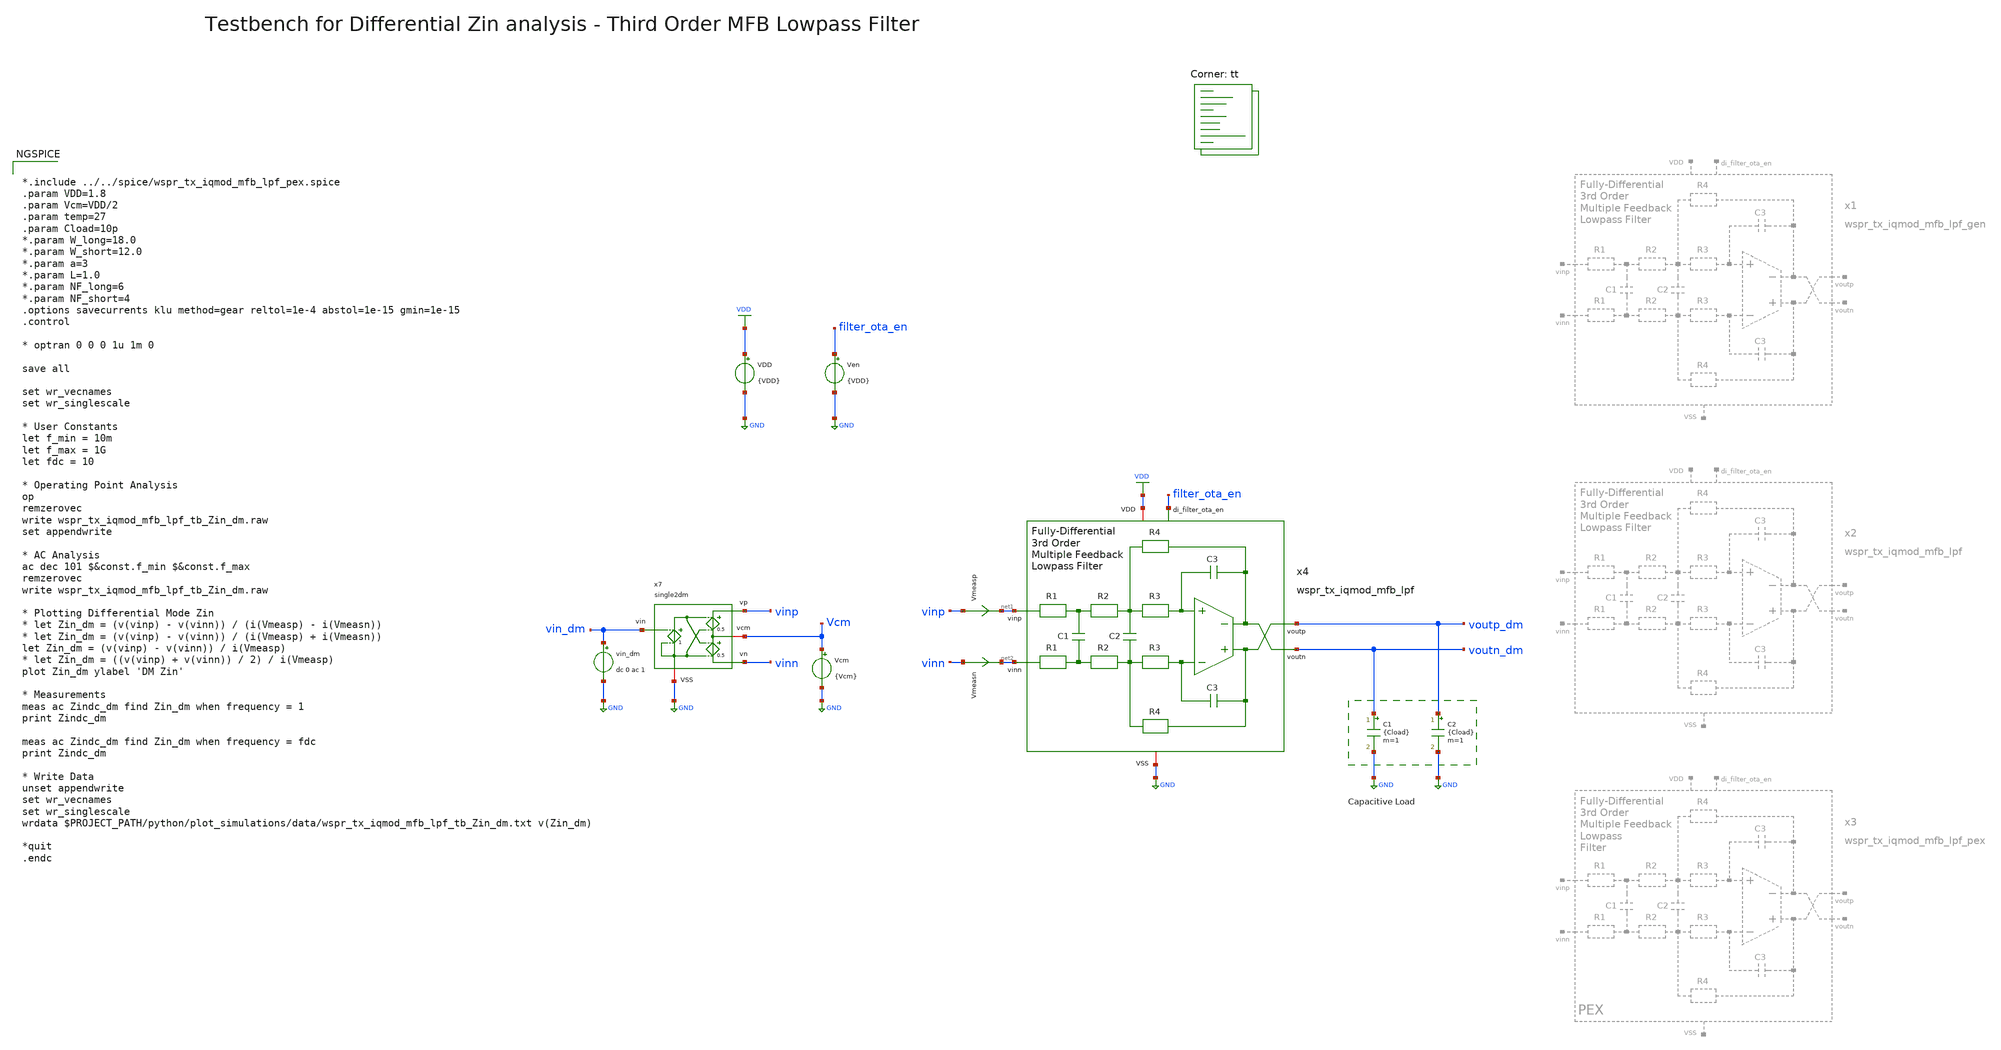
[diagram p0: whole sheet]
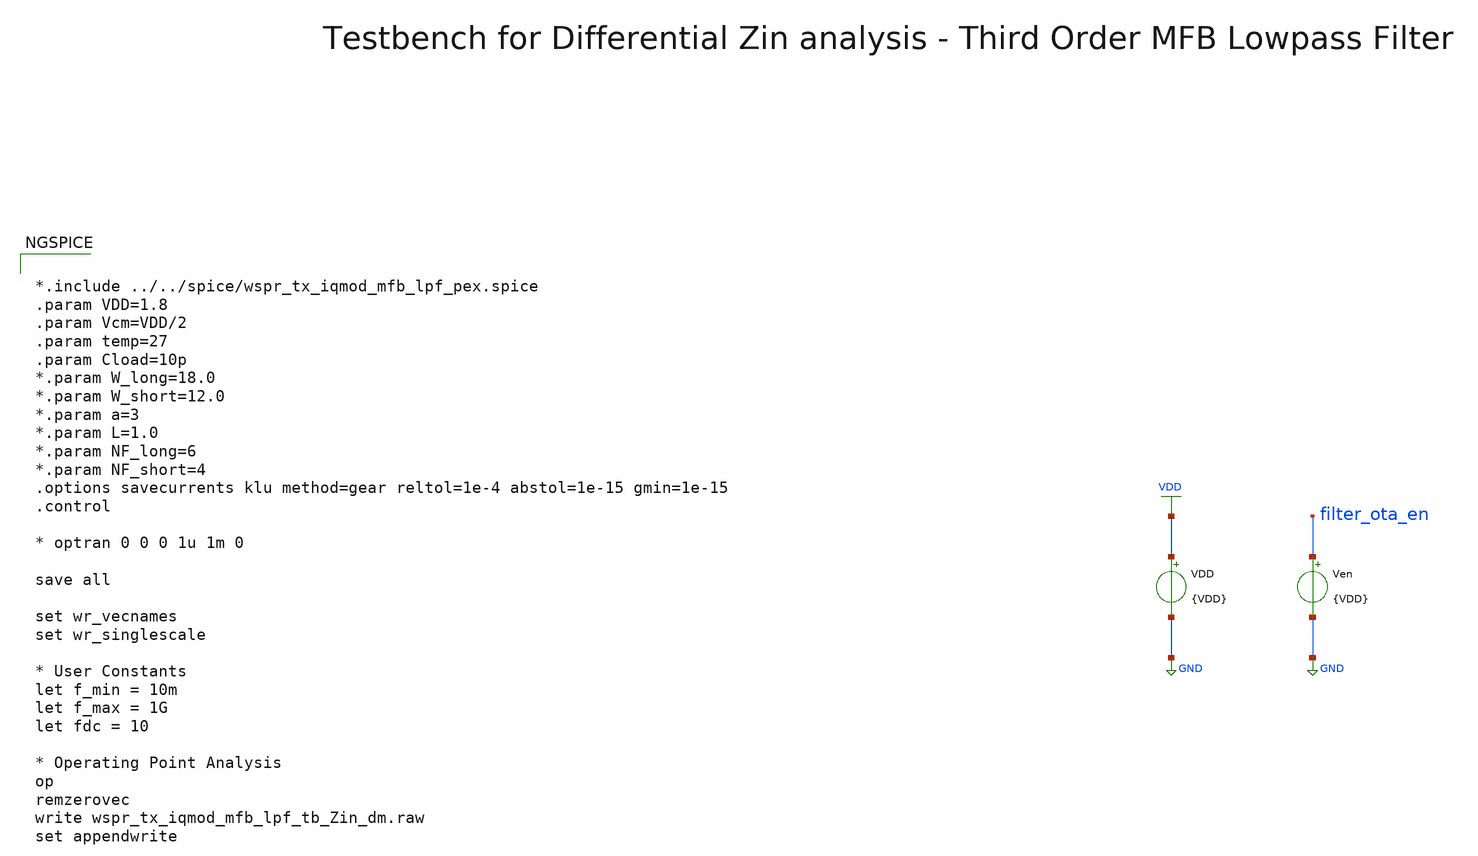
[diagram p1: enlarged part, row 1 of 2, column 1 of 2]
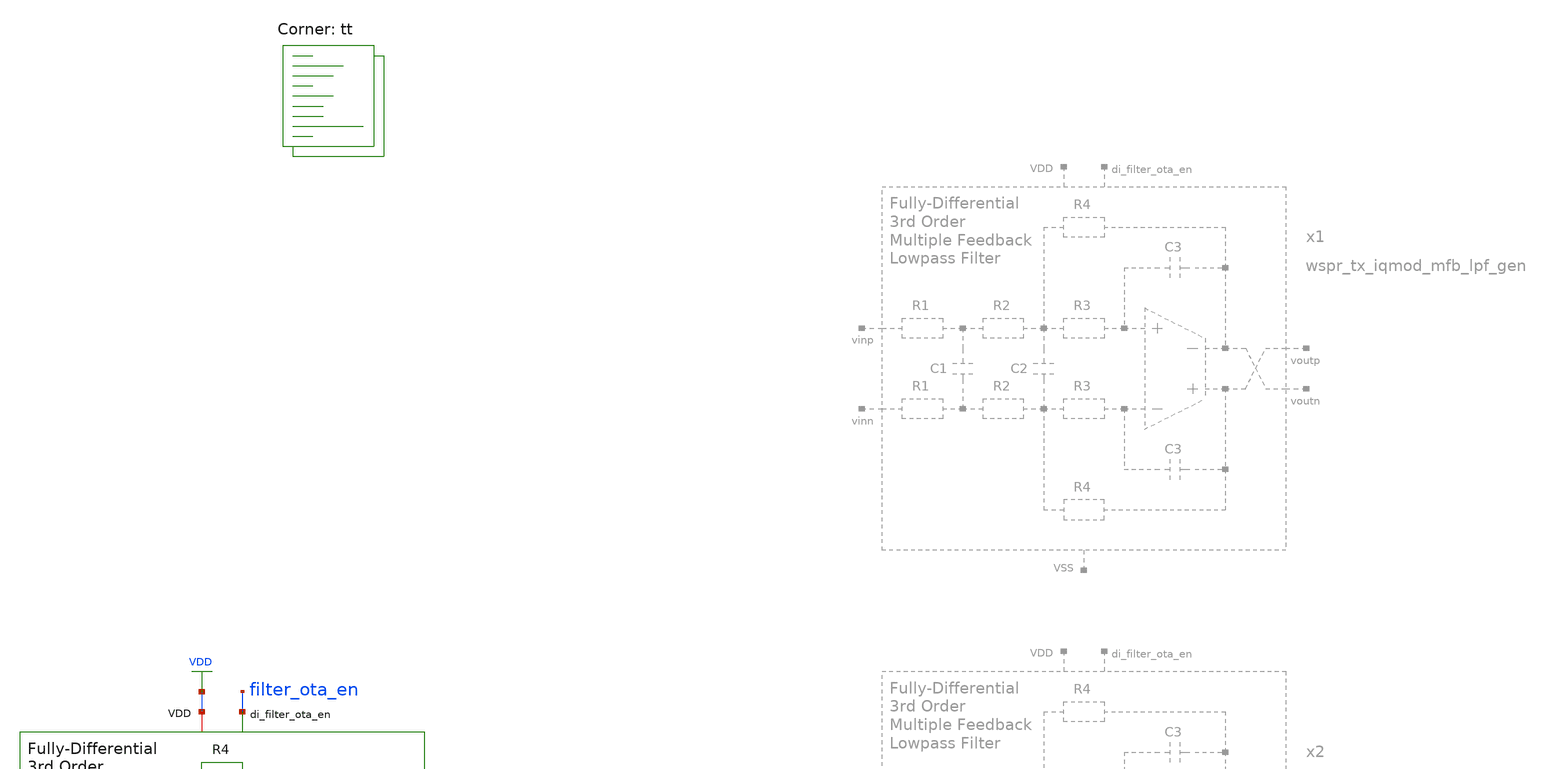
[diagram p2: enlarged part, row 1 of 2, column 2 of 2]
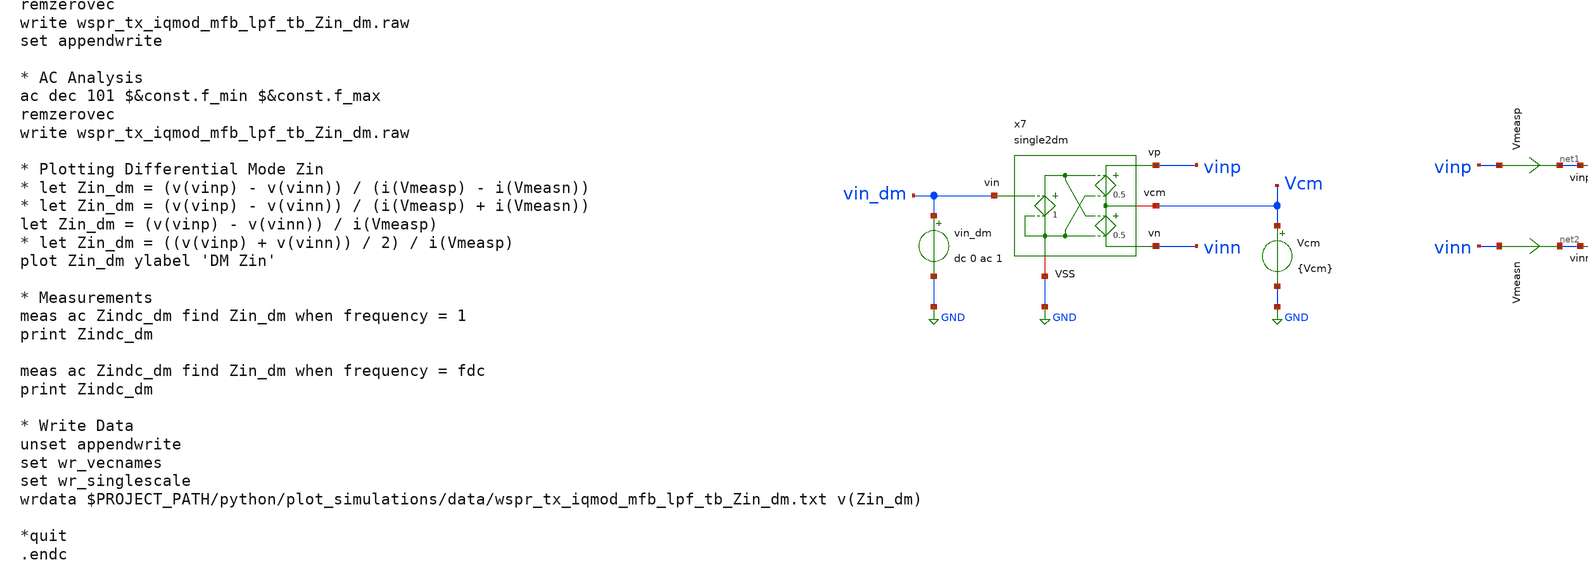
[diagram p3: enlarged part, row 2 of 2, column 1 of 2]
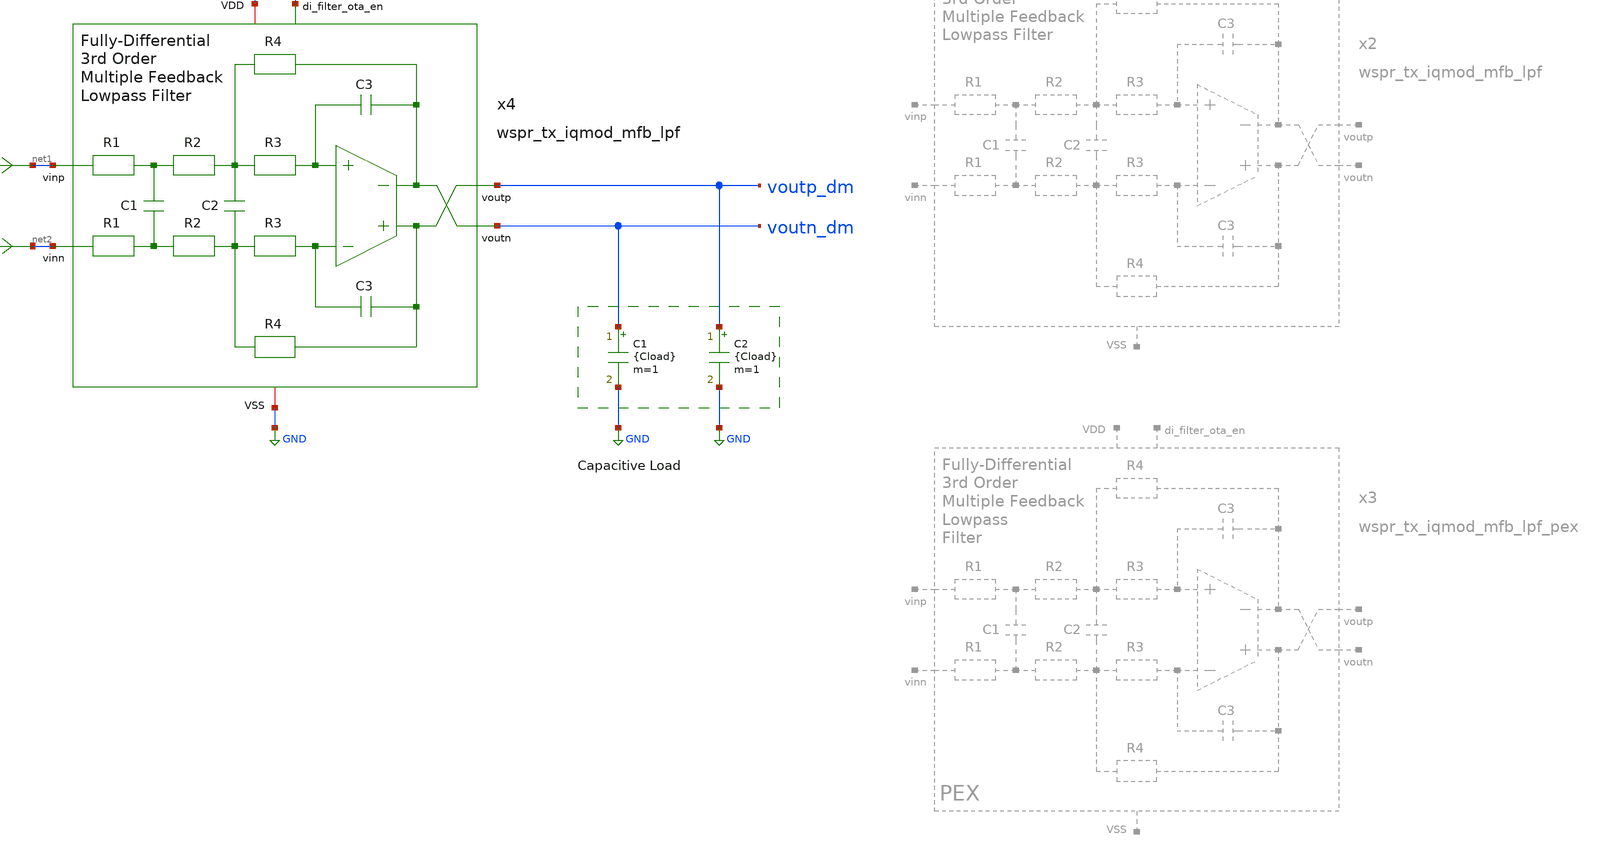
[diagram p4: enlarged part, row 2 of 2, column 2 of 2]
** sch_path: sky130/macros/iqmod/testbenches/wspr_tx_iqmod_mfb_lpf_tb_Zin_dm.sch
**.subckt wspr_tx_iqmod_mfb_lpf_tb_Zin_dm
VDD VDD GND {VDD}
C1 voutn_dm GND {Cload} m=1
C2 voutp_dm GND {Cload} m=1
Ven filter_ota_en GND {VDD}
Vmeasp vinp net1 0
.save i(vmeasp)
Vmeasn vinn net2 0
.save i(vmeasn)
Vcm Vcm GND {Vcm}
vin_dm vin_dm GND dc 0 ac 1
x4 filter_ota_en voutp_dm net1 voutn_dm net2 VDD GND wspr_tx_iqmod_mfb_lpf
x7 vinp vin_dm Vcm GND vinn single2dm
**** begin user architecture code


*.include ../../spice/wspr_tx_iqmod_mfb_lpf_pex.spice
.param VDD=1.8
.param Vcm=VDD/2
.param temp=27
.param Cload=10p
*.param W_long=18.0
*.param W_short=12.0
*.param a=3
*.param L=1.0
*.param NF_long=6
*.param NF_short=4
.options savecurrents klu method=gear reltol=1e-4 abstol=1e-15 gmin=1e-15
.control

* optran 0 0 0 1u 1m 0

save all

set wr_vecnames
set wr_singlescale

* User Constants
let f_min = 10m
let f_max = 1G
let fdc = 10

* Operating Point Analysis
op
remzerovec
write wspr_tx_iqmod_mfb_lpf_tb_Zin_dm.raw
set appendwrite

* AC Analysis
ac dec 101 $&const.f_min $&const.f_max
remzerovec
write wspr_tx_iqmod_mfb_lpf_tb_Zin_dm.raw

* Plotting Differential Mode Zin
* let Zin_dm = (v(vinp) - v(vinn)) / (i(Vmeasp) - i(Vmeasn))
* let Zin_dm = (v(vinp) - v(vinn)) / (i(Vmeasp) + i(Vmeasn))
let Zin_dm = (v(vinp) - v(vinn)) / i(Vmeasp)
* let Zin_dm = ((v(vinp) + v(vinn)) / 2) / i(Vmeasp)
plot Zin_dm ylabel 'DM Zin'

* Measurements
meas ac Zindc_dm find Zin_dm when frequency = 1
print Zindc_dm

meas ac Zindc_dm find Zin_dm when frequency = fdc
print Zindc_dm

* Write Data
unset appendwrite
set wr_vecnames
set wr_singlescale
wrdata $PROJECT_PATH/python/plot_simulations/data/wspr_tx_iqmod_mfb_lpf_tb_Zin_dm.txt v(Zin_dm)

*quit
.endc


.lib $::SKYWATER_MODELS/sky130.lib.spice tt
**** end user architecture code
**.ends
.GLOBAL GND
.GLOBAL VDD
.end
